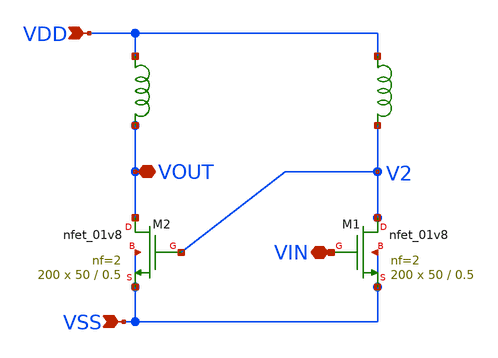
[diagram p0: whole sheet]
** sch_path: design/LELO_SVOD_SKY130A/LELO_XSC_LOOP.sch
**.subckt LELO_XSC_LOOP VSS VDD VIN VOUT
*.ipin VSS
*.ipin VDD
*.iopin VIN
*.iopin VOUT
XM1 V2 VIN VSS VSS sky130_fd_pr__nfet_01v8 L=0.5 W=50 nf=2 ad='int((nf+1)/2) * W/nf * 0.29' as='int((nf+2)/2) * W/nf * 0.29'
+ pd='2*int((nf+1)/2) * (W/nf + 0.29)' ps='2*int((nf+2)/2) * (W/nf + 0.29)' nrd='0.29 / W' nrs='0.29 / W'
+ sa=0 sb=0 sd=0 mult=200 m=200
XM2 VOUT V2 VSS VSS sky130_fd_pr__nfet_01v8 L=0.5 W=50 nf=2 ad='int((nf+1)/2) * W/nf * 0.29' as='int((nf+2)/2) * W/nf * 0.29'
+ pd='2*int((nf+1)/2) * (W/nf + 0.29)' ps='2*int((nf+2)/2) * (W/nf + 0.29)' nrd='0.29 / W' nrs='0.29 / W'
+ sa=0 sb=0 sd=0 mult=200 m=200
x1 VDD VOUT LQW2BAN3N2J00
x2 VDD V2 LQW2BAN3N2J00
**.ends

* expanding   symbol:  LELO_SVOD_SKY130A/LQW2BAN3N2J00.sym # of pins=2
** sym_path: design/LELO_SVOD_SKY130A/LQW2BAN3N2J00.sym
.SUBCKT LQW2BAN3N2J00 port1 port2
C1 port1 port2 2.87e-14
L2 port1 1 2.96e-9
R2 1 port2 1.30e-2
R3 port1 port2 4.40e+3
L4 port1 2 2.67e-8
R4 2 port2 2.47
L5 port1 3 5.23e-8
R5 3 port2 20.8
L6 port1 4 1.23e-7
R6 4 port2 692
.ENDS LQW2BAN3N2J00
.end
